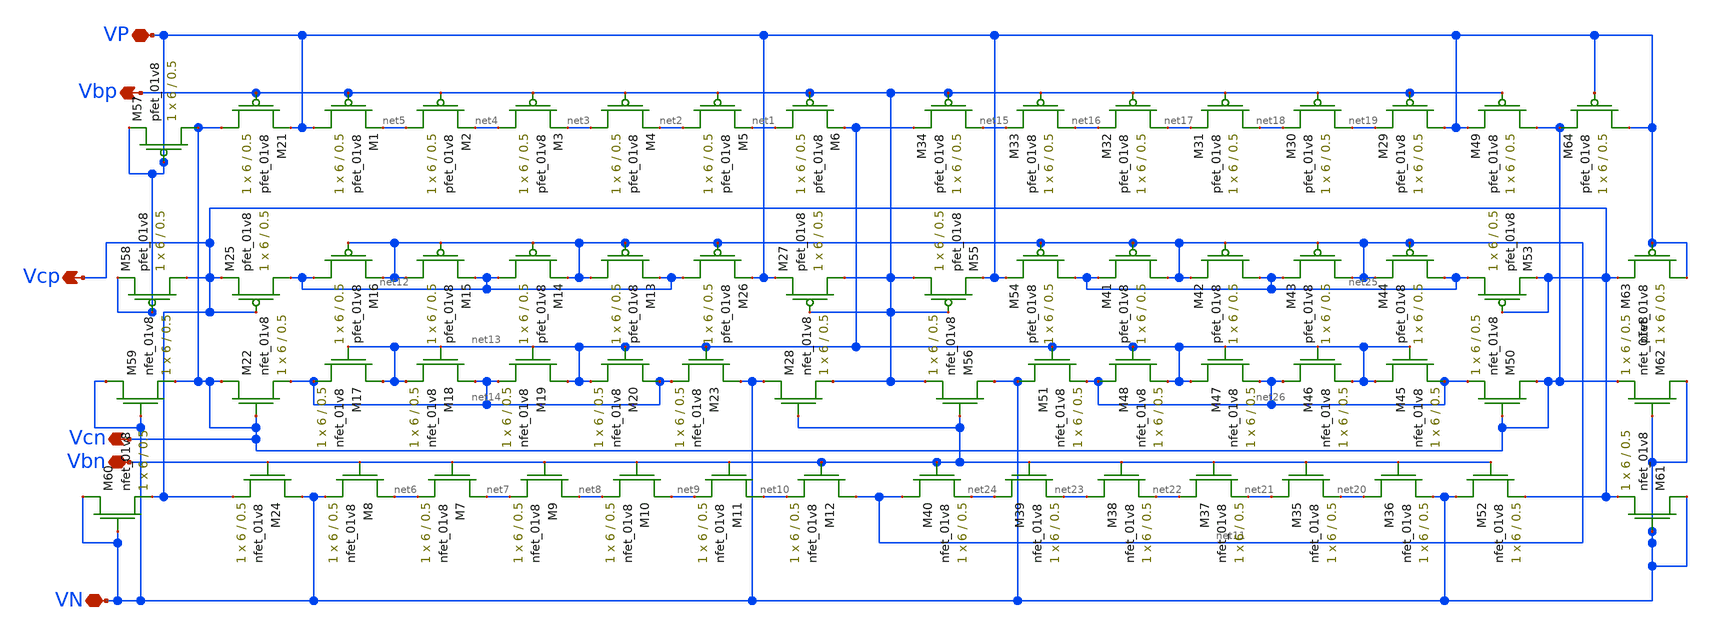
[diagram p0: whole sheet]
** sch_path: mp3/schematic/lds/bias.sch
**.subckt bias VP VN Vbn Vcn Vcp Vbp
*.iopin VP
*.iopin VN
*.iopin Vbn
*.opin Vcn
*.opin Vcp
*.opin Vbp
XM1 VP Vbp net5 VDD sky130_fd_pr__pfet_01v8 L=0.5 W=6 nf=1 ad='int((nf+1)/2) * W/nf * 0.29' as='int((nf+2)/2) * W/nf * 0.29'
+ pd='2*int((nf+1)/2) * (W/nf + 0.29)' ps='2*int((nf+2)/2) * (W/nf + 0.29)' nrd='0.29 / W' nrs='0.29 / W'
+ sa=0 sb=0 sd=0 mult=1 m=1
XM2 net5 Vbp net4 VDD sky130_fd_pr__pfet_01v8 L=0.5 W=6 nf=1 ad='int((nf+1)/2) * W/nf * 0.29' as='int((nf+2)/2) * W/nf * 0.29'
+ pd='2*int((nf+1)/2) * (W/nf + 0.29)' ps='2*int((nf+2)/2) * (W/nf + 0.29)' nrd='0.29 / W' nrs='0.29 / W'
+ sa=0 sb=0 sd=0 mult=1 m=1
XM3 net4 Vbp net3 VDD sky130_fd_pr__pfet_01v8 L=0.5 W=6 nf=1 ad='int((nf+1)/2) * W/nf * 0.29' as='int((nf+2)/2) * W/nf * 0.29'
+ pd='2*int((nf+1)/2) * (W/nf + 0.29)' ps='2*int((nf+2)/2) * (W/nf + 0.29)' nrd='0.29 / W' nrs='0.29 / W'
+ sa=0 sb=0 sd=0 mult=1 m=1
XM4 net3 Vbp net2 VDD sky130_fd_pr__pfet_01v8 L=0.5 W=6 nf=1 ad='int((nf+1)/2) * W/nf * 0.29' as='int((nf+2)/2) * W/nf * 0.29'
+ pd='2*int((nf+1)/2) * (W/nf + 0.29)' ps='2*int((nf+2)/2) * (W/nf + 0.29)' nrd='0.29 / W' nrs='0.29 / W'
+ sa=0 sb=0 sd=0 mult=1 m=1
XM5 net2 Vbp net1 VDD sky130_fd_pr__pfet_01v8 L=0.5 W=6 nf=1 ad='int((nf+1)/2) * W/nf * 0.29' as='int((nf+2)/2) * W/nf * 0.29'
+ pd='2*int((nf+1)/2) * (W/nf + 0.29)' ps='2*int((nf+2)/2) * (W/nf + 0.29)' nrd='0.29 / W' nrs='0.29 / W'
+ sa=0 sb=0 sd=0 mult=1 m=1
XM6 net1 Vbp net13 VDD sky130_fd_pr__pfet_01v8 L=0.5 W=6 nf=1 ad='int((nf+1)/2) * W/nf * 0.29' as='int((nf+2)/2) * W/nf * 0.29'
+ pd='2*int((nf+1)/2) * (W/nf + 0.29)' ps='2*int((nf+2)/2) * (W/nf + 0.29)' nrd='0.29 / W' nrs='0.29 / W'
+ sa=0 sb=0 sd=0 mult=1 m=1
XM7 net7 Vbn net6 GND sky130_fd_pr__nfet_01v8 L=0.5 W=6 nf=1 ad='int((nf+1)/2) * W/nf * 0.29' as='int((nf+2)/2) * W/nf * 0.29'
+ pd='2*int((nf+1)/2) * (W/nf + 0.29)' ps='2*int((nf+2)/2) * (W/nf + 0.29)' nrd='0.29 / W' nrs='0.29 / W'
+ sa=0 sb=0 sd=0 mult=1 m=1
XM8 net6 Vbn VN GND sky130_fd_pr__nfet_01v8 L=0.5 W=6 nf=1 ad='int((nf+1)/2) * W/nf * 0.29' as='int((nf+2)/2) * W/nf * 0.29'
+ pd='2*int((nf+1)/2) * (W/nf + 0.29)' ps='2*int((nf+2)/2) * (W/nf + 0.29)' nrd='0.29 / W' nrs='0.29 / W'
+ sa=0 sb=0 sd=0 mult=1 m=1
XM9 net8 Vbn net7 GND sky130_fd_pr__nfet_01v8 L=0.5 W=6 nf=1 ad='int((nf+1)/2) * W/nf * 0.29' as='int((nf+2)/2) * W/nf * 0.29'
+ pd='2*int((nf+1)/2) * (W/nf + 0.29)' ps='2*int((nf+2)/2) * (W/nf + 0.29)' nrd='0.29 / W' nrs='0.29 / W'
+ sa=0 sb=0 sd=0 mult=1 m=1
XM10 net9 Vbn net8 GND sky130_fd_pr__nfet_01v8 L=0.5 W=6 nf=1 ad='int((nf+1)/2) * W/nf * 0.29' as='int((nf+2)/2) * W/nf * 0.29'
+ pd='2*int((nf+1)/2) * (W/nf + 0.29)' ps='2*int((nf+2)/2) * (W/nf + 0.29)' nrd='0.29 / W' nrs='0.29 / W'
+ sa=0 sb=0 sd=0 mult=1 m=1
XM11 net10 Vbn net9 GND sky130_fd_pr__nfet_01v8 L=0.5 W=6 nf=1 ad='int((nf+1)/2) * W/nf * 0.29' as='int((nf+2)/2) * W/nf * 0.29'
+ pd='2*int((nf+1)/2) * (W/nf + 0.29)' ps='2*int((nf+2)/2) * (W/nf + 0.29)' nrd='0.29 / W' nrs='0.29 / W'
+ sa=0 sb=0 sd=0 mult=1 m=1
XM12 net11 Vbn net10 GND sky130_fd_pr__nfet_01v8 L=0.5 W=6 nf=1 ad='int((nf+1)/2) * W/nf * 0.29' as='int((nf+2)/2) * W/nf * 0.29'
+ pd='2*int((nf+1)/2) * (W/nf + 0.29)' ps='2*int((nf+2)/2) * (W/nf + 0.29)' nrd='0.29 / W' nrs='0.29 / W'
+ sa=0 sb=0 sd=0 mult=1 m=1
XM13 net11 net11 net12 VDD sky130_fd_pr__pfet_01v8 L=0.5 W=6 nf=1 ad='int((nf+1)/2) * W/nf * 0.29' as='int((nf+2)/2) * W/nf * 0.29'
+ pd='2*int((nf+1)/2) * (W/nf + 0.29)' ps='2*int((nf+2)/2) * (W/nf + 0.29)' nrd='0.29 / W' nrs='0.29 / W'
+ sa=0 sb=0 sd=0 mult=1 m=1
XM14 net12 net11 net11 VDD sky130_fd_pr__pfet_01v8 L=0.5 W=6 nf=1 ad='int((nf+1)/2) * W/nf * 0.29' as='int((nf+2)/2) * W/nf * 0.29'
+ pd='2*int((nf+1)/2) * (W/nf + 0.29)' ps='2*int((nf+2)/2) * (W/nf + 0.29)' nrd='0.29 / W' nrs='0.29 / W'
+ sa=0 sb=0 sd=0 mult=1 m=1
XM15 net11 net11 net12 VDD sky130_fd_pr__pfet_01v8 L=0.5 W=6 nf=1 ad='int((nf+1)/2) * W/nf * 0.29' as='int((nf+2)/2) * W/nf * 0.29'
+ pd='2*int((nf+1)/2) * (W/nf + 0.29)' ps='2*int((nf+2)/2) * (W/nf + 0.29)' nrd='0.29 / W' nrs='0.29 / W'
+ sa=0 sb=0 sd=0 mult=1 m=1
XM16 net12 net11 net11 VDD sky130_fd_pr__pfet_01v8 L=0.5 W=6 nf=1 ad='int((nf+1)/2) * W/nf * 0.29' as='int((nf+2)/2) * W/nf * 0.29'
+ pd='2*int((nf+1)/2) * (W/nf + 0.29)' ps='2*int((nf+2)/2) * (W/nf + 0.29)' nrd='0.29 / W' nrs='0.29 / W'
+ sa=0 sb=0 sd=0 mult=1 m=1
XM17 net13 net13 net14 GND sky130_fd_pr__nfet_01v8 L=0.5 W=6 nf=1 ad='int((nf+1)/2) * W/nf * 0.29' as='int((nf+2)/2) * W/nf * 0.29'
+ pd='2*int((nf+1)/2) * (W/nf + 0.29)' ps='2*int((nf+2)/2) * (W/nf + 0.29)' nrd='0.29 / W' nrs='0.29 / W'
+ sa=0 sb=0 sd=0 mult=1 m=1
XM18 net14 net13 net13 GND sky130_fd_pr__nfet_01v8 L=0.5 W=6 nf=1 ad='int((nf+1)/2) * W/nf * 0.29' as='int((nf+2)/2) * W/nf * 0.29'
+ pd='2*int((nf+1)/2) * (W/nf + 0.29)' ps='2*int((nf+2)/2) * (W/nf + 0.29)' nrd='0.29 / W' nrs='0.29 / W'
+ sa=0 sb=0 sd=0 mult=1 m=1
XM19 net13 net13 net14 GND sky130_fd_pr__nfet_01v8 L=0.5 W=6 nf=1 ad='int((nf+1)/2) * W/nf * 0.29' as='int((nf+2)/2) * W/nf * 0.29'
+ pd='2*int((nf+1)/2) * (W/nf + 0.29)' ps='2*int((nf+2)/2) * (W/nf + 0.29)' nrd='0.29 / W' nrs='0.29 / W'
+ sa=0 sb=0 sd=0 mult=1 m=1
XM20 net14 net13 net13 GND sky130_fd_pr__nfet_01v8 L=0.5 W=6 nf=1 ad='int((nf+1)/2) * W/nf * 0.29' as='int((nf+2)/2) * W/nf * 0.29'
+ pd='2*int((nf+1)/2) * (W/nf + 0.29)' ps='2*int((nf+2)/2) * (W/nf + 0.29)' nrd='0.29 / W' nrs='0.29 / W'
+ sa=0 sb=0 sd=0 mult=1 m=1
XM21 Vcn Vbp VP VDD sky130_fd_pr__pfet_01v8 L=0.5 W=6 nf=1 ad='int((nf+1)/2) * W/nf * 0.29' as='int((nf+2)/2) * W/nf * 0.29'
+ pd='2*int((nf+1)/2) * (W/nf + 0.29)' ps='2*int((nf+2)/2) * (W/nf + 0.29)' nrd='0.29 / W' nrs='0.29 / W'
+ sa=0 sb=0 sd=0 mult=1 m=1
XM22 Vcn Vcn net14 GND sky130_fd_pr__nfet_01v8 L=0.5 W=6 nf=1 ad='int((nf+1)/2) * W/nf * 0.29' as='int((nf+2)/2) * W/nf * 0.29'
+ pd='2*int((nf+1)/2) * (W/nf + 0.29)' ps='2*int((nf+2)/2) * (W/nf + 0.29)' nrd='0.29 / W' nrs='0.29 / W'
+ sa=0 sb=0 sd=0 mult=1 m=1
XM23 VN net13 net14 GND sky130_fd_pr__nfet_01v8 L=0.5 W=6 nf=1 ad='int((nf+1)/2) * W/nf * 0.29' as='int((nf+2)/2) * W/nf * 0.29'
+ pd='2*int((nf+1)/2) * (W/nf + 0.29)' ps='2*int((nf+2)/2) * (W/nf + 0.29)' nrd='0.29 / W' nrs='0.29 / W'
+ sa=0 sb=0 sd=0 mult=1 m=1
XM24 VN Vbn Vcp GND sky130_fd_pr__nfet_01v8 L=0.5 W=6 nf=1 ad='int((nf+1)/2) * W/nf * 0.29' as='int((nf+2)/2) * W/nf * 0.29'
+ pd='2*int((nf+1)/2) * (W/nf + 0.29)' ps='2*int((nf+2)/2) * (W/nf + 0.29)' nrd='0.29 / W' nrs='0.29 / W'
+ sa=0 sb=0 sd=0 mult=1 m=1
XM25 net12 Vcp Vcp VDD sky130_fd_pr__pfet_01v8 L=0.5 W=6 nf=1 ad='int((nf+1)/2) * W/nf * 0.29' as='int((nf+2)/2) * W/nf * 0.29'
+ pd='2*int((nf+1)/2) * (W/nf + 0.29)' ps='2*int((nf+2)/2) * (W/nf + 0.29)' nrd='0.29 / W' nrs='0.29 / W'
+ sa=0 sb=0 sd=0 mult=1 m=1
XM26 net12 net11 VP VDD sky130_fd_pr__pfet_01v8 L=0.5 W=6 nf=1 ad='int((nf+1)/2) * W/nf * 0.29' as='int((nf+2)/2) * W/nf * 0.29'
+ pd='2*int((nf+1)/2) * (W/nf + 0.29)' ps='2*int((nf+2)/2) * (W/nf + 0.29)' nrd='0.29 / W' nrs='0.29 / W'
+ sa=0 sb=0 sd=0 mult=1 m=1
XM27 Vbp Vbp VP VDD sky130_fd_pr__pfet_01v8 L=0.5 W=6 nf=1 ad='int((nf+1)/2) * W/nf * 0.29' as='int((nf+2)/2) * W/nf * 0.29'
+ pd='2*int((nf+1)/2) * (W/nf + 0.29)' ps='2*int((nf+2)/2) * (W/nf + 0.29)' nrd='0.29 / W' nrs='0.29 / W'
+ sa=0 sb=0 sd=0 mult=1 m=1
XM28 VN Vbn Vbp GND sky130_fd_pr__nfet_01v8 L=0.5 W=6 nf=1 ad='int((nf+1)/2) * W/nf * 0.29' as='int((nf+2)/2) * W/nf * 0.29'
+ pd='2*int((nf+1)/2) * (W/nf + 0.29)' ps='2*int((nf+2)/2) * (W/nf + 0.29)' nrd='0.29 / W' nrs='0.29 / W'
+ sa=0 sb=0 sd=0 mult=1 m=1
XM29 VP Vbp net19 VDD sky130_fd_pr__pfet_01v8 L=0.5 W=6 nf=1 ad='int((nf+1)/2) * W/nf * 0.29' as='int((nf+2)/2) * W/nf * 0.29'
+ pd='2*int((nf+1)/2) * (W/nf + 0.29)' ps='2*int((nf+2)/2) * (W/nf + 0.29)' nrd='0.29 / W' nrs='0.29 / W'
+ sa=0 sb=0 sd=0 mult=1 m=1
XM30 net19 Vbp net18 VDD sky130_fd_pr__pfet_01v8 L=0.5 W=6 nf=1 ad='int((nf+1)/2) * W/nf * 0.29' as='int((nf+2)/2) * W/nf * 0.29'
+ pd='2*int((nf+1)/2) * (W/nf + 0.29)' ps='2*int((nf+2)/2) * (W/nf + 0.29)' nrd='0.29 / W' nrs='0.29 / W'
+ sa=0 sb=0 sd=0 mult=1 m=1
XM31 net18 Vbp net17 VDD sky130_fd_pr__pfet_01v8 L=0.5 W=6 nf=1 ad='int((nf+1)/2) * W/nf * 0.29' as='int((nf+2)/2) * W/nf * 0.29'
+ pd='2*int((nf+1)/2) * (W/nf + 0.29)' ps='2*int((nf+2)/2) * (W/nf + 0.29)' nrd='0.29 / W' nrs='0.29 / W'
+ sa=0 sb=0 sd=0 mult=1 m=1
XM32 net17 Vbp net16 VDD sky130_fd_pr__pfet_01v8 L=0.5 W=6 nf=1 ad='int((nf+1)/2) * W/nf * 0.29' as='int((nf+2)/2) * W/nf * 0.29'
+ pd='2*int((nf+1)/2) * (W/nf + 0.29)' ps='2*int((nf+2)/2) * (W/nf + 0.29)' nrd='0.29 / W' nrs='0.29 / W'
+ sa=0 sb=0 sd=0 mult=1 m=1
XM33 net16 Vbp net15 VDD sky130_fd_pr__pfet_01v8 L=0.5 W=6 nf=1 ad='int((nf+1)/2) * W/nf * 0.29' as='int((nf+2)/2) * W/nf * 0.29'
+ pd='2*int((nf+1)/2) * (W/nf + 0.29)' ps='2*int((nf+2)/2) * (W/nf + 0.29)' nrd='0.29 / W' nrs='0.29 / W'
+ sa=0 sb=0 sd=0 mult=1 m=1
XM34 net15 Vbp net13 VDD sky130_fd_pr__pfet_01v8 L=0.5 W=6 nf=1 ad='int((nf+1)/2) * W/nf * 0.29' as='int((nf+2)/2) * W/nf * 0.29'
+ pd='2*int((nf+1)/2) * (W/nf + 0.29)' ps='2*int((nf+2)/2) * (W/nf + 0.29)' nrd='0.29 / W' nrs='0.29 / W'
+ sa=0 sb=0 sd=0 mult=1 m=1
XM35 net21 Vbn net20 GND sky130_fd_pr__nfet_01v8 L=0.5 W=6 nf=1 ad='int((nf+1)/2) * W/nf * 0.29' as='int((nf+2)/2) * W/nf * 0.29'
+ pd='2*int((nf+1)/2) * (W/nf + 0.29)' ps='2*int((nf+2)/2) * (W/nf + 0.29)' nrd='0.29 / W' nrs='0.29 / W'
+ sa=0 sb=0 sd=0 mult=1 m=1
XM36 net20 Vbn VN GND sky130_fd_pr__nfet_01v8 L=0.5 W=6 nf=1 ad='int((nf+1)/2) * W/nf * 0.29' as='int((nf+2)/2) * W/nf * 0.29'
+ pd='2*int((nf+1)/2) * (W/nf + 0.29)' ps='2*int((nf+2)/2) * (W/nf + 0.29)' nrd='0.29 / W' nrs='0.29 / W'
+ sa=0 sb=0 sd=0 mult=1 m=1
XM37 net22 Vbn net21 GND sky130_fd_pr__nfet_01v8 L=0.5 W=6 nf=1 ad='int((nf+1)/2) * W/nf * 0.29' as='int((nf+2)/2) * W/nf * 0.29'
+ pd='2*int((nf+1)/2) * (W/nf + 0.29)' ps='2*int((nf+2)/2) * (W/nf + 0.29)' nrd='0.29 / W' nrs='0.29 / W'
+ sa=0 sb=0 sd=0 mult=1 m=1
XM38 net23 Vbn net22 GND sky130_fd_pr__nfet_01v8 L=0.5 W=6 nf=1 ad='int((nf+1)/2) * W/nf * 0.29' as='int((nf+2)/2) * W/nf * 0.29'
+ pd='2*int((nf+1)/2) * (W/nf + 0.29)' ps='2*int((nf+2)/2) * (W/nf + 0.29)' nrd='0.29 / W' nrs='0.29 / W'
+ sa=0 sb=0 sd=0 mult=1 m=1
XM39 net24 Vbn net23 GND sky130_fd_pr__nfet_01v8 L=0.5 W=6 nf=1 ad='int((nf+1)/2) * W/nf * 0.29' as='int((nf+2)/2) * W/nf * 0.29'
+ pd='2*int((nf+1)/2) * (W/nf + 0.29)' ps='2*int((nf+2)/2) * (W/nf + 0.29)' nrd='0.29 / W' nrs='0.29 / W'
+ sa=0 sb=0 sd=0 mult=1 m=1
XM40 net11 Vbn net24 GND sky130_fd_pr__nfet_01v8 L=0.5 W=6 nf=1 ad='int((nf+1)/2) * W/nf * 0.29' as='int((nf+2)/2) * W/nf * 0.29'
+ pd='2*int((nf+1)/2) * (W/nf + 0.29)' ps='2*int((nf+2)/2) * (W/nf + 0.29)' nrd='0.29 / W' nrs='0.29 / W'
+ sa=0 sb=0 sd=0 mult=1 m=1
XM41 net11 net11 net25 VDD sky130_fd_pr__pfet_01v8 L=0.5 W=6 nf=1 ad='int((nf+1)/2) * W/nf * 0.29' as='int((nf+2)/2) * W/nf * 0.29'
+ pd='2*int((nf+1)/2) * (W/nf + 0.29)' ps='2*int((nf+2)/2) * (W/nf + 0.29)' nrd='0.29 / W' nrs='0.29 / W'
+ sa=0 sb=0 sd=0 mult=1 m=1
XM42 net25 net11 net11 VDD sky130_fd_pr__pfet_01v8 L=0.5 W=6 nf=1 ad='int((nf+1)/2) * W/nf * 0.29' as='int((nf+2)/2) * W/nf * 0.29'
+ pd='2*int((nf+1)/2) * (W/nf + 0.29)' ps='2*int((nf+2)/2) * (W/nf + 0.29)' nrd='0.29 / W' nrs='0.29 / W'
+ sa=0 sb=0 sd=0 mult=1 m=1
XM43 net11 net11 net25 VDD sky130_fd_pr__pfet_01v8 L=0.5 W=6 nf=1 ad='int((nf+1)/2) * W/nf * 0.29' as='int((nf+2)/2) * W/nf * 0.29'
+ pd='2*int((nf+1)/2) * (W/nf + 0.29)' ps='2*int((nf+2)/2) * (W/nf + 0.29)' nrd='0.29 / W' nrs='0.29 / W'
+ sa=0 sb=0 sd=0 mult=1 m=1
XM44 net25 net11 net11 VDD sky130_fd_pr__pfet_01v8 L=0.5 W=6 nf=1 ad='int((nf+1)/2) * W/nf * 0.29' as='int((nf+2)/2) * W/nf * 0.29'
+ pd='2*int((nf+1)/2) * (W/nf + 0.29)' ps='2*int((nf+2)/2) * (W/nf + 0.29)' nrd='0.29 / W' nrs='0.29 / W'
+ sa=0 sb=0 sd=0 mult=1 m=1
XM45 net13 net13 net26 GND sky130_fd_pr__nfet_01v8 L=0.5 W=6 nf=1 ad='int((nf+1)/2) * W/nf * 0.29' as='int((nf+2)/2) * W/nf * 0.29'
+ pd='2*int((nf+1)/2) * (W/nf + 0.29)' ps='2*int((nf+2)/2) * (W/nf + 0.29)' nrd='0.29 / W' nrs='0.29 / W'
+ sa=0 sb=0 sd=0 mult=1 m=1
XM46 net26 net13 net13 GND sky130_fd_pr__nfet_01v8 L=0.5 W=6 nf=1 ad='int((nf+1)/2) * W/nf * 0.29' as='int((nf+2)/2) * W/nf * 0.29'
+ pd='2*int((nf+1)/2) * (W/nf + 0.29)' ps='2*int((nf+2)/2) * (W/nf + 0.29)' nrd='0.29 / W' nrs='0.29 / W'
+ sa=0 sb=0 sd=0 mult=1 m=1
XM47 net13 net13 net26 GND sky130_fd_pr__nfet_01v8 L=0.5 W=6 nf=1 ad='int((nf+1)/2) * W/nf * 0.29' as='int((nf+2)/2) * W/nf * 0.29'
+ pd='2*int((nf+1)/2) * (W/nf + 0.29)' ps='2*int((nf+2)/2) * (W/nf + 0.29)' nrd='0.29 / W' nrs='0.29 / W'
+ sa=0 sb=0 sd=0 mult=1 m=1
XM48 net26 net13 net13 GND sky130_fd_pr__nfet_01v8 L=0.5 W=6 nf=1 ad='int((nf+1)/2) * W/nf * 0.29' as='int((nf+2)/2) * W/nf * 0.29'
+ pd='2*int((nf+1)/2) * (W/nf + 0.29)' ps='2*int((nf+2)/2) * (W/nf + 0.29)' nrd='0.29 / W' nrs='0.29 / W'
+ sa=0 sb=0 sd=0 mult=1 m=1
XM49 Vcn Vbp VP VDD sky130_fd_pr__pfet_01v8 L=0.5 W=6 nf=1 ad='int((nf+1)/2) * W/nf * 0.29' as='int((nf+2)/2) * W/nf * 0.29'
+ pd='2*int((nf+1)/2) * (W/nf + 0.29)' ps='2*int((nf+2)/2) * (W/nf + 0.29)' nrd='0.29 / W' nrs='0.29 / W'
+ sa=0 sb=0 sd=0 mult=1 m=1
XM50 Vcn Vcn net26 GND sky130_fd_pr__nfet_01v8 L=0.5 W=6 nf=1 ad='int((nf+1)/2) * W/nf * 0.29' as='int((nf+2)/2) * W/nf * 0.29'
+ pd='2*int((nf+1)/2) * (W/nf + 0.29)' ps='2*int((nf+2)/2) * (W/nf + 0.29)' nrd='0.29 / W' nrs='0.29 / W'
+ sa=0 sb=0 sd=0 mult=1 m=1
XM51 VN net13 net26 GND sky130_fd_pr__nfet_01v8 L=0.5 W=6 nf=1 ad='int((nf+1)/2) * W/nf * 0.29' as='int((nf+2)/2) * W/nf * 0.29'
+ pd='2*int((nf+1)/2) * (W/nf + 0.29)' ps='2*int((nf+2)/2) * (W/nf + 0.29)' nrd='0.29 / W' nrs='0.29 / W'
+ sa=0 sb=0 sd=0 mult=1 m=1
XM52 VN Vbn Vcp GND sky130_fd_pr__nfet_01v8 L=0.5 W=6 nf=1 ad='int((nf+1)/2) * W/nf * 0.29' as='int((nf+2)/2) * W/nf * 0.29'
+ pd='2*int((nf+1)/2) * (W/nf + 0.29)' ps='2*int((nf+2)/2) * (W/nf + 0.29)' nrd='0.29 / W' nrs='0.29 / W'
+ sa=0 sb=0 sd=0 mult=1 m=1
XM53 net25 Vcp Vcp VDD sky130_fd_pr__pfet_01v8 L=0.5 W=6 nf=1 ad='int((nf+1)/2) * W/nf * 0.29' as='int((nf+2)/2) * W/nf * 0.29'
+ pd='2*int((nf+1)/2) * (W/nf + 0.29)' ps='2*int((nf+2)/2) * (W/nf + 0.29)' nrd='0.29 / W' nrs='0.29 / W'
+ sa=0 sb=0 sd=0 mult=1 m=1
XM54 net25 net11 VP VDD sky130_fd_pr__pfet_01v8 L=0.5 W=6 nf=1 ad='int((nf+1)/2) * W/nf * 0.29' as='int((nf+2)/2) * W/nf * 0.29'
+ pd='2*int((nf+1)/2) * (W/nf + 0.29)' ps='2*int((nf+2)/2) * (W/nf + 0.29)' nrd='0.29 / W' nrs='0.29 / W'
+ sa=0 sb=0 sd=0 mult=1 m=1
XM55 Vbp Vbp VP VDD sky130_fd_pr__pfet_01v8 L=0.5 W=6 nf=1 ad='int((nf+1)/2) * W/nf * 0.29' as='int((nf+2)/2) * W/nf * 0.29'
+ pd='2*int((nf+1)/2) * (W/nf + 0.29)' ps='2*int((nf+2)/2) * (W/nf + 0.29)' nrd='0.29 / W' nrs='0.29 / W'
+ sa=0 sb=0 sd=0 mult=1 m=1
XM56 VN Vbn Vbp GND sky130_fd_pr__nfet_01v8 L=0.5 W=6 nf=1 ad='int((nf+1)/2) * W/nf * 0.29' as='int((nf+2)/2) * W/nf * 0.29'
+ pd='2*int((nf+1)/2) * (W/nf + 0.29)' ps='2*int((nf+2)/2) * (W/nf + 0.29)' nrd='0.29 / W' nrs='0.29 / W'
+ sa=0 sb=0 sd=0 mult=1 m=1
XM57 Vcn VP VP VDD sky130_fd_pr__pfet_01v8 L=0.5 W=6 nf=1 ad='int((nf+1)/2) * W/nf * 0.29' as='int((nf+2)/2) * W/nf * 0.29'
+ pd='2*int((nf+1)/2) * (W/nf + 0.29)' ps='2*int((nf+2)/2) * (W/nf + 0.29)' nrd='0.29 / W' nrs='0.29 / W'
+ sa=0 sb=0 sd=0 mult=1 m=1
XM58 Vcp VP VP VDD sky130_fd_pr__pfet_01v8 L=0.5 W=6 nf=1 ad='int((nf+1)/2) * W/nf * 0.29' as='int((nf+2)/2) * W/nf * 0.29'
+ pd='2*int((nf+1)/2) * (W/nf + 0.29)' ps='2*int((nf+2)/2) * (W/nf + 0.29)' nrd='0.29 / W' nrs='0.29 / W'
+ sa=0 sb=0 sd=0 mult=1 m=1
XM59 VN VN Vcn GND sky130_fd_pr__nfet_01v8 L=0.5 W=6 nf=1 ad='int((nf+1)/2) * W/nf * 0.29' as='int((nf+2)/2) * W/nf * 0.29'
+ pd='2*int((nf+1)/2) * (W/nf + 0.29)' ps='2*int((nf+2)/2) * (W/nf + 0.29)' nrd='0.29 / W' nrs='0.29 / W'
+ sa=0 sb=0 sd=0 mult=1 m=1
XM60 VN VN Vcp GND sky130_fd_pr__nfet_01v8 L=0.5 W=6 nf=1 ad='int((nf+1)/2) * W/nf * 0.29' as='int((nf+2)/2) * W/nf * 0.29'
+ pd='2*int((nf+1)/2) * (W/nf + 0.29)' ps='2*int((nf+2)/2) * (W/nf + 0.29)' nrd='0.29 / W' nrs='0.29 / W'
+ sa=0 sb=0 sd=0 mult=1 m=1
XM61 VN VN Vcp GND sky130_fd_pr__nfet_01v8 L=0.5 W=6 nf=1 ad='int((nf+1)/2) * W/nf * 0.29' as='int((nf+2)/2) * W/nf * 0.29'
+ pd='2*int((nf+1)/2) * (W/nf + 0.29)' ps='2*int((nf+2)/2) * (W/nf + 0.29)' nrd='0.29 / W' nrs='0.29 / W'
+ sa=0 sb=0 sd=0 mult=1 m=1
XM62 VN VN Vcn GND sky130_fd_pr__nfet_01v8 L=0.5 W=6 nf=1 ad='int((nf+1)/2) * W/nf * 0.29' as='int((nf+2)/2) * W/nf * 0.29'
+ pd='2*int((nf+1)/2) * (W/nf + 0.29)' ps='2*int((nf+2)/2) * (W/nf + 0.29)' nrd='0.29 / W' nrs='0.29 / W'
+ sa=0 sb=0 sd=0 mult=1 m=1
XM63 VP VP Vcp VDD sky130_fd_pr__pfet_01v8 L=0.5 W=6 nf=1 ad='int((nf+1)/2) * W/nf * 0.29' as='int((nf+2)/2) * W/nf * 0.29'
+ pd='2*int((nf+1)/2) * (W/nf + 0.29)' ps='2*int((nf+2)/2) * (W/nf + 0.29)' nrd='0.29 / W' nrs='0.29 / W'
+ sa=0 sb=0 sd=0 mult=1 m=1
XM64 VP VP Vcn VDD sky130_fd_pr__pfet_01v8 L=0.5 W=6 nf=1 ad='int((nf+1)/2) * W/nf * 0.29' as='int((nf+2)/2) * W/nf * 0.29'
+ pd='2*int((nf+1)/2) * (W/nf + 0.29)' ps='2*int((nf+2)/2) * (W/nf + 0.29)' nrd='0.29 / W' nrs='0.29 / W'
+ sa=0 sb=0 sd=0 mult=1 m=1
**.ends
.end
